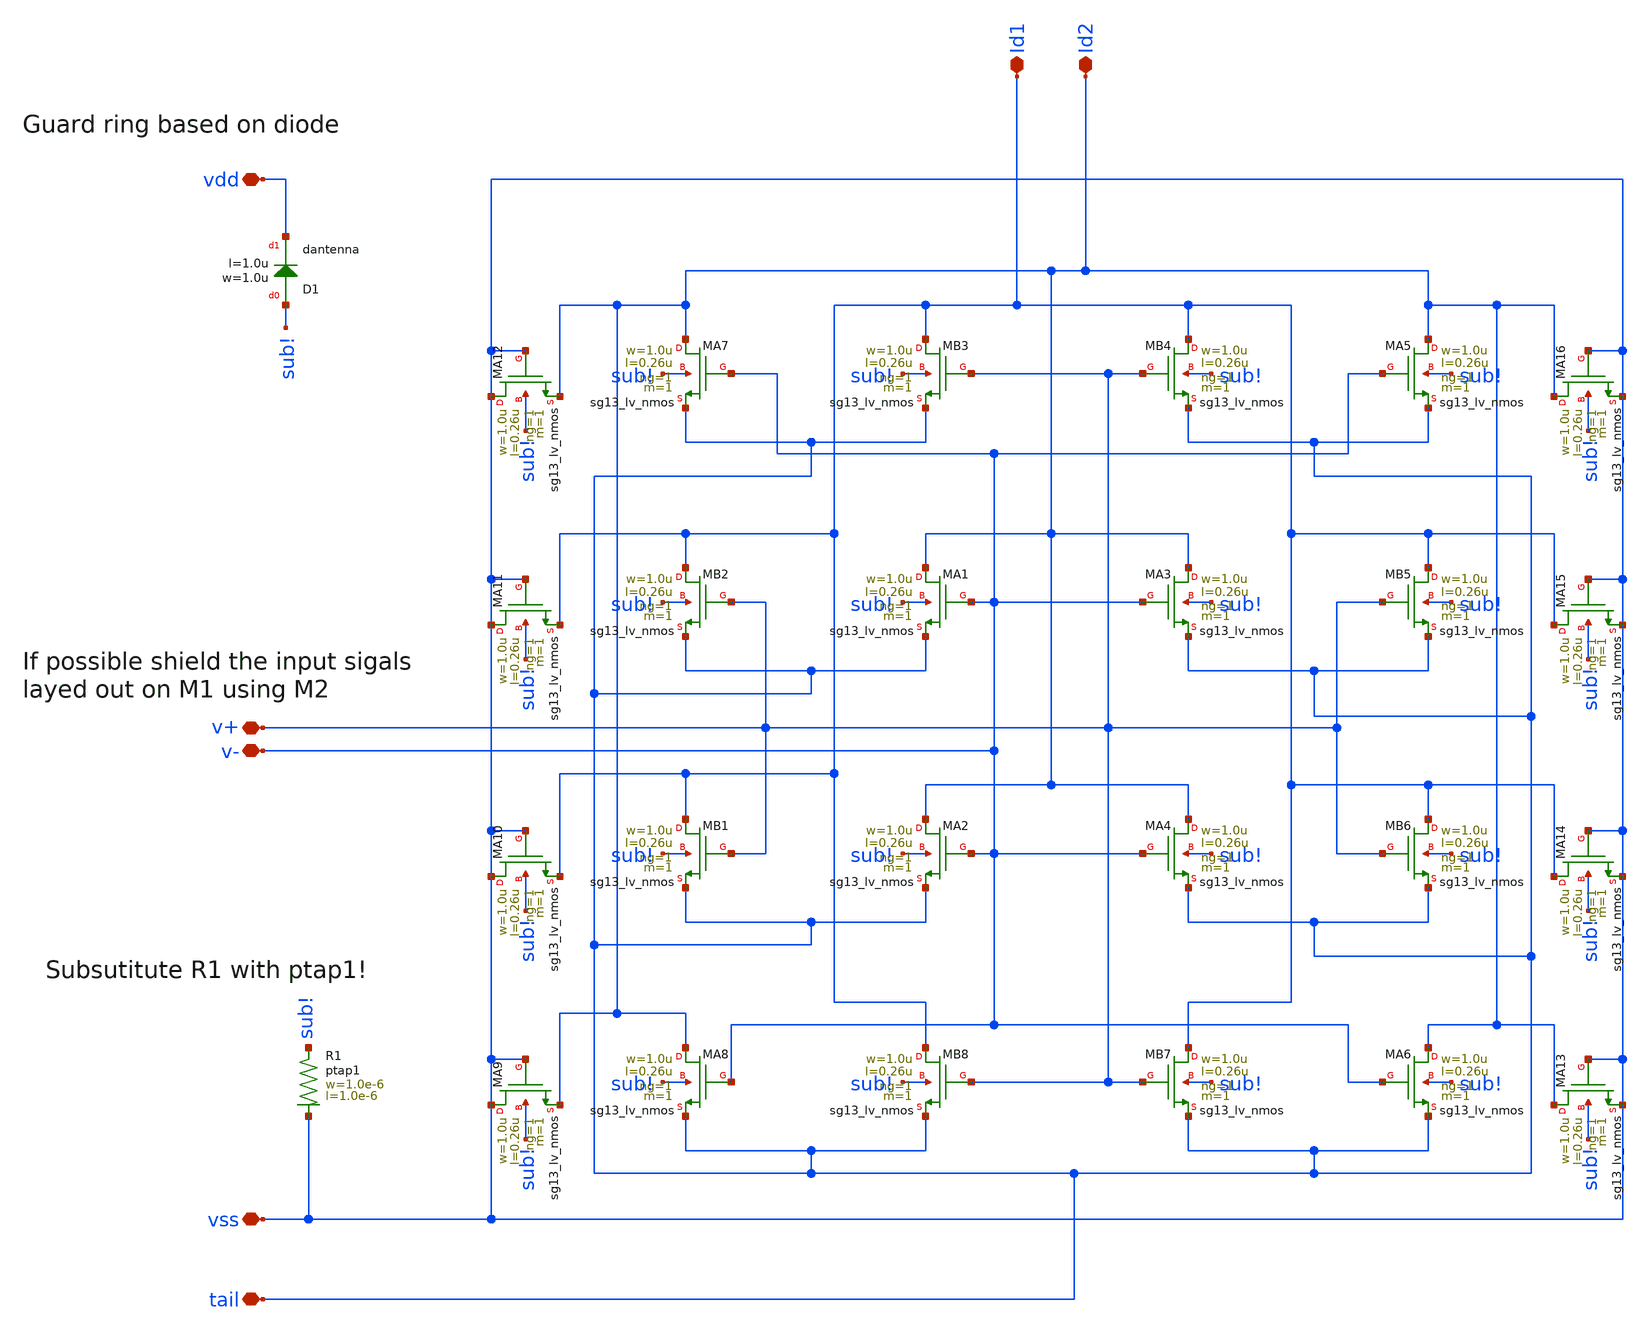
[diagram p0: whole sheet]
** sch_path: CMP7345-main/schematic/xschem/diff_pair.sch
**.subckt diff_pair v- v+ vss tail Id2 Id1 vdd
*.iopin v-
*.iopin v+
*.iopin vss
*.iopin tail
*.iopin Id2
*.iopin Id1
*.iopin vdd
XMA1 Id2 v- tail sub! sg13_lv_nmos w=1.0u l=0.26u ng=1 m=1 mm_ok=0
XMA2 Id2 v- tail sub! sg13_lv_nmos w=1.0u l=0.26u ng=1 m=1 mm_ok=0
XMA3 Id2 v- tail sub! sg13_lv_nmos w=1.0u l=0.26u ng=1 m=1 mm_ok=0
XMA4 Id2 v- tail sub! sg13_lv_nmos w=1.0u l=0.26u ng=1 m=1 mm_ok=0
XMB1 Id1 v+ tail sub! sg13_lv_nmos w=1.0u l=0.26u ng=1 m=1 mm_ok=0
XMB2 Id1 v+ tail sub! sg13_lv_nmos w=1.0u l=0.26u ng=1 m=1 mm_ok=0
XMB3 Id1 v+ tail sub! sg13_lv_nmos w=1.0u l=0.26u ng=1 m=1 mm_ok=0
XMB4 Id1 v+ tail sub! sg13_lv_nmos w=1.0u l=0.26u ng=1 m=1 mm_ok=0
XMA5 Id2 v- tail sub! sg13_lv_nmos w=1.0u l=0.26u ng=1 m=1 mm_ok=0
XMA6 Id2 v- tail sub! sg13_lv_nmos w=1.0u l=0.26u ng=1 m=1 mm_ok=0
XMA7 Id2 v- tail sub! sg13_lv_nmos w=1.0u l=0.26u ng=1 m=1 mm_ok=0
XMA8 Id2 v- tail sub! sg13_lv_nmos w=1.0u l=0.26u ng=1 m=1 mm_ok=0
XMB5 Id1 v+ tail sub! sg13_lv_nmos w=1.0u l=0.26u ng=1 m=1 mm_ok=0
XMB6 Id1 v+ tail sub! sg13_lv_nmos w=1.0u l=0.26u ng=1 m=1 mm_ok=0
XMB7 Id1 v+ tail sub! sg13_lv_nmos w=1.0u l=0.26u ng=1 m=1 mm_ok=0
XMB8 Id1 v+ tail sub! sg13_lv_nmos w=1.0u l=0.26u ng=1 m=1 mm_ok=0
XMA9 vss vss Id2 sub! sg13_lv_nmos w=1.0u l=0.26u ng=1 m=1 mm_ok=0
XMA10 vss vss Id1 sub! sg13_lv_nmos w=1.0u l=0.26u ng=1 m=1 mm_ok=0
XMA11 vss vss Id1 sub! sg13_lv_nmos w=1.0u l=0.26u ng=1 m=1 mm_ok=0
XMA12 vss vss Id2 sub! sg13_lv_nmos w=1.0u l=0.26u ng=1 m=1 mm_ok=0
XMA13 Id2 vss vss sub! sg13_lv_nmos w=1.0u l=0.26u ng=1 m=1 mm_ok=0
XMA14 Id1 vss vss sub! sg13_lv_nmos w=1.0u l=0.26u ng=1 m=1 mm_ok=0
XMA15 Id1 vss vss sub! sg13_lv_nmos w=1.0u l=0.26u ng=1 m=1 mm_ok=0
XMA16 Id2 vss vss sub! sg13_lv_nmos w=1.0u l=0.26u ng=1 m=1 mm_ok=0
XR1 sub! vss ptap1 R=196 w=1.0e-6 l=1.0e-6
XD1 sub! vdd dantenna l=1.0u w=1.0u
**.ends
.end
